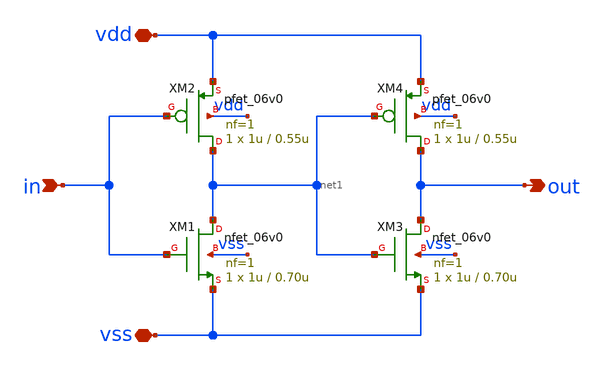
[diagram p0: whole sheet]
** sch_path: xschem/logic/buffer_lvt.sch
**.subckt buffer_lvt vdd vss in out
*.iopin vdd
*.iopin vss
*.ipin in
*.opin out
XM1 net1 in vss vss nfet_06v0 L=0.70u W=1u nf=1 ad='int((nf+1)/2) * W/nf * 0.18u' as='int((nf+2)/2) * W/nf * 0.18u'
+ pd='2*int((nf+1)/2) * (W/nf + 0.18u)' ps='2*int((nf+2)/2) * (W/nf + 0.18u)' nrd='0.18u / W' nrs='0.18u / W'
+ sa=0 sb=0 sd=0 m=1
XM2 net1 in vdd vdd pfet_06v0 L=0.55u W=1u nf=1 ad='int((nf+1)/2) * W/nf * 0.18u' as='int((nf+2)/2) * W/nf * 0.18u'
+ pd='2*int((nf+1)/2) * (W/nf + 0.18u)' ps='2*int((nf+2)/2) * (W/nf + 0.18u)' nrd='0.18u / W' nrs='0.18u / W'
+ sa=0 sb=0 sd=0 m=1
XM3 out net1 vss vss nfet_06v0 L=0.70u W=1u nf=1 ad='int((nf+1)/2) * W/nf * 0.18u' as='int((nf+2)/2) * W/nf * 0.18u'
+ pd='2*int((nf+1)/2) * (W/nf + 0.18u)' ps='2*int((nf+2)/2) * (W/nf + 0.18u)' nrd='0.18u / W' nrs='0.18u / W'
+ sa=0 sb=0 sd=0 m=1
XM4 out net1 vdd vdd pfet_06v0 L=0.55u W=1u nf=1 ad='int((nf+1)/2) * W/nf * 0.18u' as='int((nf+2)/2) * W/nf * 0.18u'
+ pd='2*int((nf+1)/2) * (W/nf + 0.18u)' ps='2*int((nf+2)/2) * (W/nf + 0.18u)' nrd='0.18u / W' nrs='0.18u / W'
+ sa=0 sb=0 sd=0 m=1
**.ends
.end
